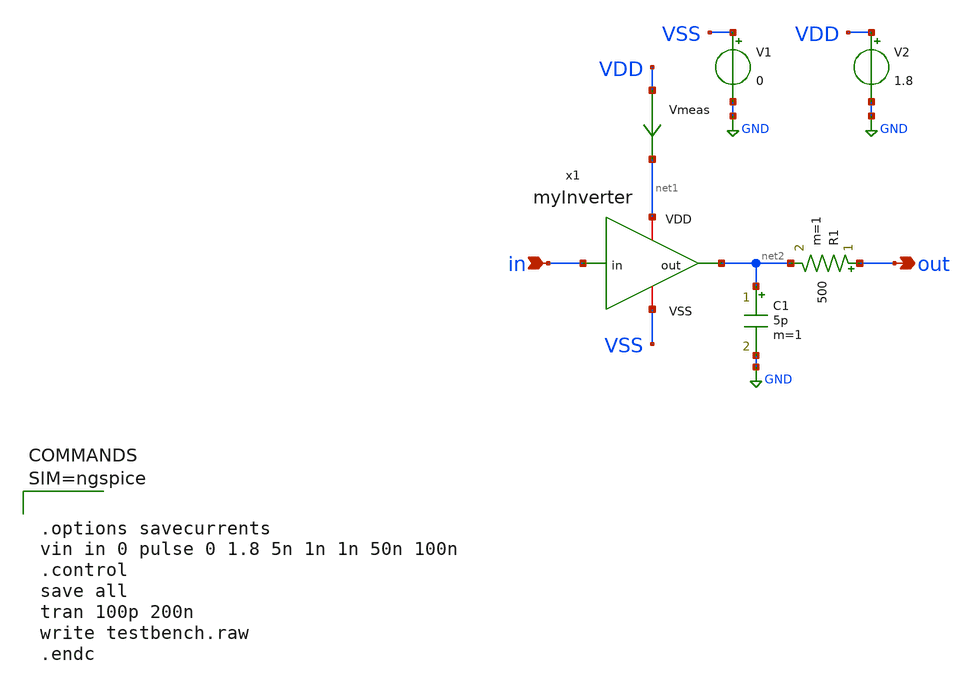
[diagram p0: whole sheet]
** sch_path: xschem/testbench.sch
**.subckt testbench in out
*.ipin in
*.opin out
x1 VSS net1 net2 in myInverter
V1 VSS GND 0
V2 VDD GND 1.8
R1 out net2 500 m=1
C1 net2 GND 5p m=1
Vmeas VDD net1 0
.save i(vmeas)
**** begin user architecture code

** opencircuitdesign pdks install
.lib $::SKYWATER_MODELS/sky130.lib.spice tt





.options savecurrents
vin in 0 pulse 0 1.8 5n 1n 1n 50n 100n
.control
save all
tran 100p 200n
write testbench.raw
.endc



**** end user architecture code
**.ends

* expanding   symbol:  myInverter.sym # of pins=4
** sym_path: xschem/myInverter.sym
** sch_path: xschem/myInverter.sch
.subckt myInverter VSS VDD out in
*.iopin VDD
*.iopin VSS
*.ipin in
*.opin out
XM2 out in VSS VSS sky130_fd_pr__nfet_01v8 L=0.15 W=1 nf=1 ad='int((nf+1)/2) * W/nf * 0.29' as='int((nf+2)/2) * W/nf * 0.29'
+ pd='2*int((nf+1)/2) * (W/nf + 0.29)' ps='2*int((nf+2)/2) * (W/nf + 0.29)' nrd='0.29 / W' nrs='0.29 / W'
+ sa=0 sb=0 sd=0 mult=1 m=1
XM1 out in VDD VDD sky130_fd_pr__pfet_01v8 L=0.15 W=2 nf=1 ad='int((nf+1)/2) * W/nf * 0.29' as='int((nf+2)/2) * W/nf * 0.29'
+ pd='2*int((nf+1)/2) * (W/nf + 0.29)' ps='2*int((nf+2)/2) * (W/nf + 0.29)' nrd='0.29 / W' nrs='0.29 / W'
+ sa=0 sb=0 sd=0 mult=1 m=1
.ends

.GLOBAL GND
.end
